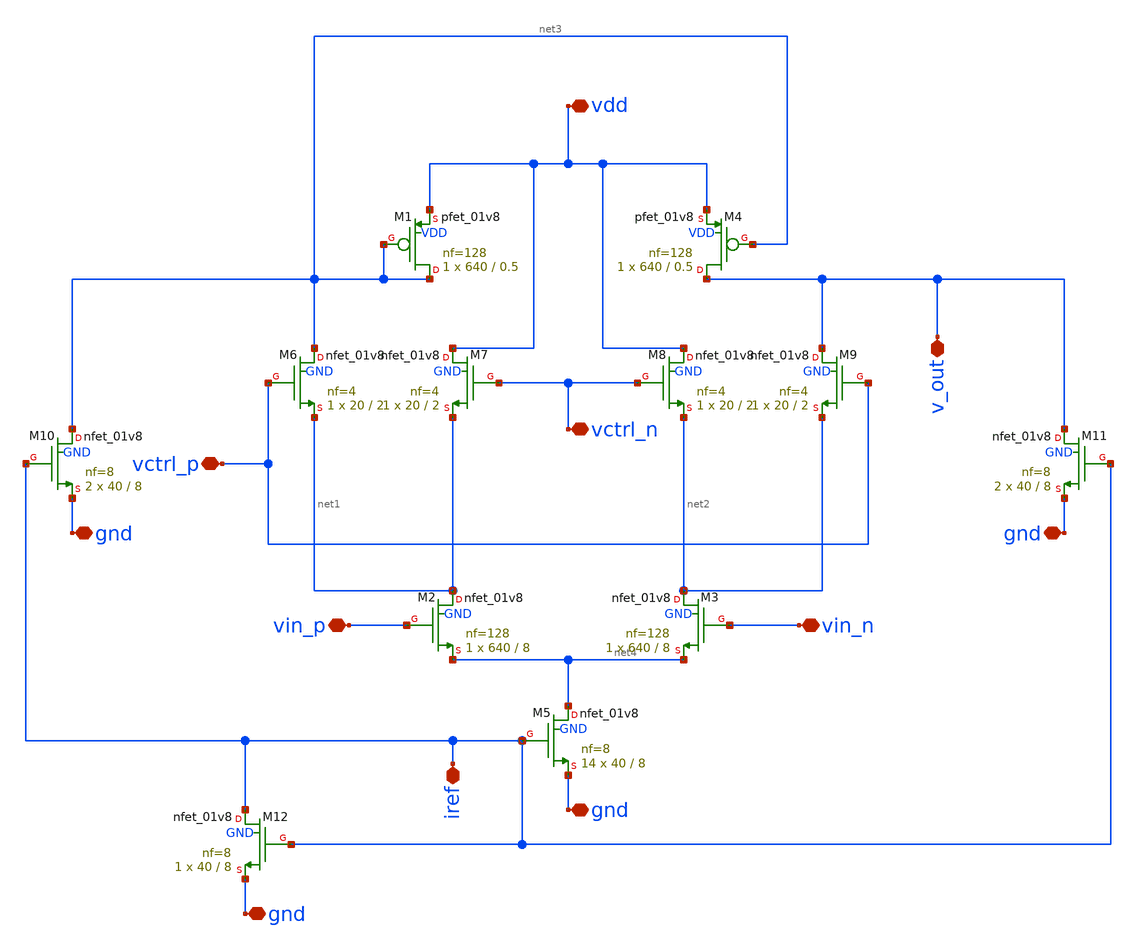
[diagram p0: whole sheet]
** sch_path: ISSCC27/submitted_notebooks/subthreshold_vga_gmid/schematic/vga_core_12t.sch
**.subckt vga_core_12t vdd vin_n iref vctrl_n gnd gnd vctrl_p vin_p v_out gnd gnd
*.iopin vdd
*.iopin vin_n
*.iopin iref
*.iopin vctrl_n
*.iopin gnd
*.iopin gnd
*.iopin vctrl_p
*.iopin vin_p
*.iopin v_out
*.iopin gnd
*.iopin gnd
XM1 net3 net3 vdd VDD sky130_fd_pr__pfet_01v8 L=0.5 W=640 nf=128 ad='int((128 + 1)/2) * 640 / 128 * 0.29'
+ as='int((128 + 2)/2) * 640 / 128 * 0.29' pd='2*int((128 + 1)/2) * (640 / 128 + 0.29)' ps='2*int((128 + 2)/2) * (640 / 128 + 0.29)'
+ nrd='0.29 / 640 ' nrs='0.29 / 640 ' sa=0 sb=0 sd=0 mult=1 m=1
XM2 net1 vin_p net4 GND sky130_fd_pr__nfet_01v8 L=8 W=640 nf=128 ad='int((128 + 1)/2) * 640 / 128 * 0.29'
+ as='int((128 + 2)/2) * 640 / 128 * 0.29' pd='2*int((128 + 1)/2) * (640 / 128 + 0.29)' ps='2*int((128 + 2)/2) * (640 / 128 + 0.29)'
+ nrd='0.29 / 640 ' nrs='0.29 / 640 ' sa=0 sb=0 sd=0 mult=1 m=1
XM3 net2 vin_n net4 GND sky130_fd_pr__nfet_01v8 L=8 W=640 nf=128 ad='int((128 + 1)/2) * 640 / 128 * 0.29'
+ as='int((128 + 2)/2) * 640 / 128 * 0.29' pd='2*int((128 + 1)/2) * (640 / 128 + 0.29)' ps='2*int((128 + 2)/2) * (640 / 128 + 0.29)'
+ nrd='0.29 / 640 ' nrs='0.29 / 640 ' sa=0 sb=0 sd=0 mult=1 m=1
XM4 v_out net3 vdd VDD sky130_fd_pr__pfet_01v8 L=0.5 W=640 nf=128 ad='int((128 + 1)/2) * 640 / 128 * 0.29'
+ as='int((128 + 2)/2) * 640 / 128 * 0.29' pd='2*int((128 + 1)/2) * (640 / 128 + 0.29)' ps='2*int((128 + 2)/2) * (640 / 128 + 0.29)'
+ nrd='0.29 / 640 ' nrs='0.29 / 640 ' sa=0 sb=0 sd=0 mult=1 m=1
XM5 net4 iref gnd GND sky130_fd_pr__nfet_01v8 L=8 W=40 nf=8 ad='int((8 + 1)/2) * 40 / 8 * 0.29' as='int((8 + 2)/2) * 40 / 8 * 0.29'
+ pd='2*int((8 + 1)/2) * (40 / 8 + 0.29)' ps='2*int((8 + 2)/2) * (40 / 8 + 0.29)' nrd='0.29 / 40 ' nrs='0.29 / 40 '
+ sa=0 sb=0 sd=0 mult=14 m=14
XM6 net3 vctrl_p net1 GND sky130_fd_pr__nfet_01v8 L=2 W=20 nf=4 ad='int((4 + 1)/2) * 20 / 4 * 0.29' as='int((4 + 2)/2) * 20 / 4 * 0.29'
+ pd='2*int((4 + 1)/2) * (20 / 4 + 0.29)' ps='2*int((4 + 2)/2) * (20 / 4 + 0.29)' nrd='0.29 / 20 ' nrs='0.29 / 20 '
+ sa=0 sb=0 sd=0 mult=1 m=1
XM7 vdd vctrl_n net1 GND sky130_fd_pr__nfet_01v8 L=2 W=20 nf=4 ad='int((4 + 1)/2) * 20 / 4 * 0.29' as='int((4 + 2)/2) * 20 / 4 * 0.29'
+ pd='2*int((4 + 1)/2) * (20 / 4 + 0.29)' ps='2*int((4 + 2)/2) * (20 / 4 + 0.29)' nrd='0.29 / 20 ' nrs='0.29 / 20 '
+ sa=0 sb=0 sd=0 mult=1 m=1
XM8 vdd vctrl_n net2 GND sky130_fd_pr__nfet_01v8 L=2 W=20 nf=4 ad='int((4 + 1)/2) * 20 / 4 * 0.29' as='int((4 + 2)/2) * 20 / 4 * 0.29'
+ pd='2*int((4 + 1)/2) * (20 / 4 + 0.29)' ps='2*int((4 + 2)/2) * (20 / 4 + 0.29)' nrd='0.29 / 20 ' nrs='0.29 / 20 '
+ sa=0 sb=0 sd=0 mult=1 m=1
XM9 v_out vctrl_p net2 GND sky130_fd_pr__nfet_01v8 L=2 W=20 nf=4 ad='int((4 + 1)/2) * 20 / 4 * 0.29'
+ as='int((4 + 2)/2) * 20 / 4 * 0.29' pd='2*int((4 + 1)/2) * (20 / 4 + 0.29)' ps='2*int((4 + 2)/2) * (20 / 4 + 0.29)'
+ nrd='0.29 / 20 ' nrs='0.29 / 20 ' sa=0 sb=0 sd=0 mult=1 m=1
XM10 net3 iref gnd GND sky130_fd_pr__nfet_01v8 L=8 W=40 nf=8 ad='int((8 + 1)/2) * 40 / 8 * 0.29' as='int((8 + 2)/2) * 40 / 8 * 0.29'
+ pd='2*int((8 + 1)/2) * (40 / 8 + 0.29)' ps='2*int((8 + 2)/2) * (40 / 8 + 0.29)' nrd='0.29 / 40 ' nrs='0.29 / 40 '
+ sa=0 sb=0 sd=0 mult=2 m=2
XM11 v_out iref gnd GND sky130_fd_pr__nfet_01v8 L=8 W=40 nf=8 ad='int((8 + 1)/2) * 40 / 8 * 0.29' as='int((8 + 2)/2) * 40 / 8 * 0.29'
+ pd='2*int((8 + 1)/2) * (40 / 8 + 0.29)' ps='2*int((8 + 2)/2) * (40 / 8 + 0.29)' nrd='0.29 / 40 ' nrs='0.29 / 40 '
+ sa=0 sb=0 sd=0 mult=2 m=2
XM12 iref iref gnd GND sky130_fd_pr__nfet_01v8 L=8 W=40 nf=8 ad='int((8 + 1)/2) * 40 / 8 * 0.29' as='int((8 + 2)/2) * 40 / 8 * 0.29'
+ pd='2*int((8 + 1)/2) * (40 / 8 + 0.29)' ps='2*int((8 + 2)/2) * (40 / 8 + 0.29)' nrd='0.29 / 40 ' nrs='0.29 / 40 '
+ sa=0 sb=0 sd=0 mult=1 m=1
**.ends
.end
